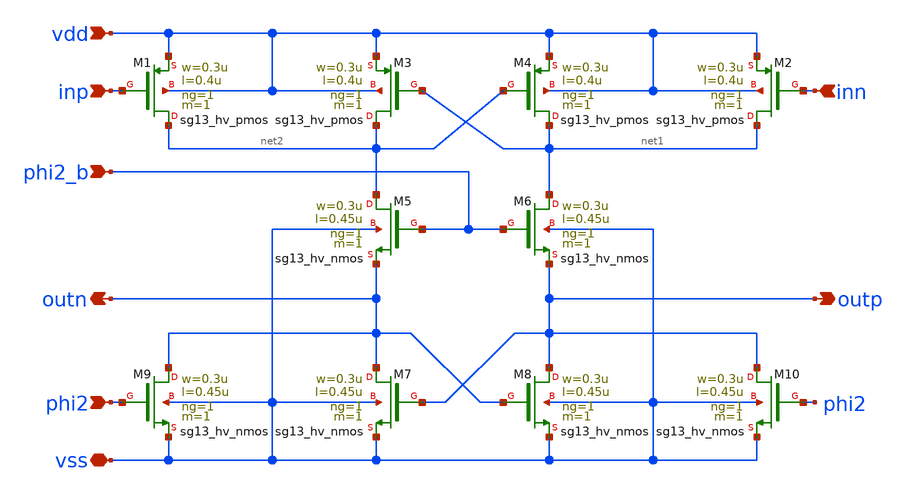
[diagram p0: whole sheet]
** sch_path: 3_real_circuits/comparator_latched.sch
**.subckt comparator_latched inp vdd inn outp outn phi2_b phi2 vss
*.ipin inp
*.ipin vdd
*.ipin inn
*.opin outp
*.opin outn
*.ipin phi2_b
*.ipin phi2
*.iopin vss
XM9 outn phi2 vss vss sg13_hv_nmos w=0.3u l=0.45u ng=1 m=1 mm_ok=1
XM7 outn outp vss vss sg13_hv_nmos w=0.3u l=0.45u ng=1 m=1 mm_ok=1
XM8 outp outn vss vss sg13_hv_nmos w=0.3u l=0.45u ng=1 m=1 mm_ok=1
XM10 outp phi2 vss vss sg13_hv_nmos w=0.3u l=0.45u ng=1 m=1 mm_ok=1
XM5 net2 phi2_b outn vss sg13_hv_nmos w=0.3u l=0.45u ng=1 m=1 mm_ok=1
XM6 net1 phi2_b outp vss sg13_hv_nmos w=0.3u l=0.45u ng=1 m=1 mm_ok=1
XM1 net2 inp vdd vdd sg13_hv_pmos w=0.3u l=0.4u ng=1 m=1 mm_ok=1
XM3 net2 net1 vdd vdd sg13_hv_pmos w=0.3u l=0.4u ng=1 m=1 mm_ok=1
XM4 net1 net2 vdd vdd sg13_hv_pmos w=0.3u l=0.4u ng=1 m=1 mm_ok=1
XM2 net1 inn vdd vdd sg13_hv_pmos w=0.3u l=0.4u ng=1 m=1 mm_ok=1
**.ends
.end
